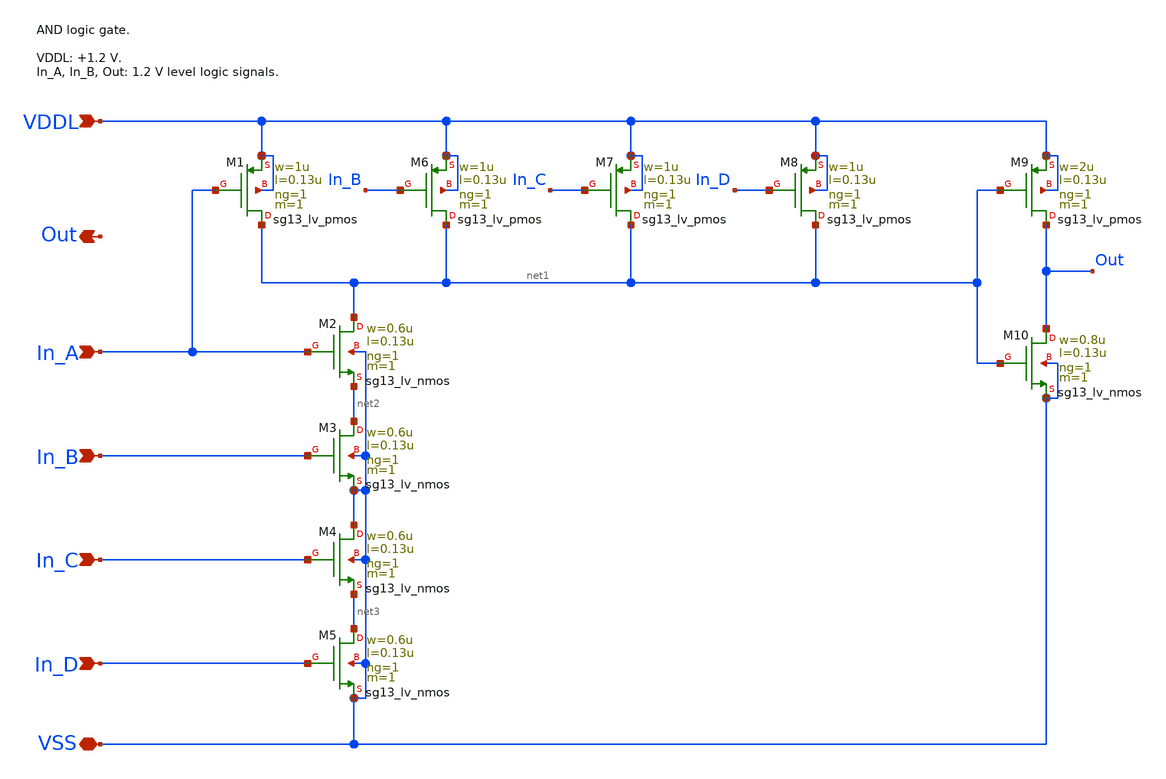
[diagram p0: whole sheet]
** sch_path: sar_adc/xschem/blocks/logic_elements/4-input_AND/4-input_AND.sch
**.subckt 4-input_AND Out VSS VDDL In_A In_B In_C In_D
*.opin Out
*.iopin VSS
*.ipin VDDL
*.ipin In_A
*.ipin In_B
*.ipin In_C
*.ipin In_D
XM1 net1 In_A VDDL VDDL sg13_lv_pmos w=1u l=0.13u ng=1 m=1 mm_ok=1
XM6 net1 In_B VDDL VDDL sg13_lv_pmos w=1u l=0.13u ng=1 m=1 mm_ok=1
XM2 net1 In_A net2 VSS sg13_lv_nmos w=0.6u l=0.13u ng=1 m=1 mm_ok=1
XM3 net2 In_B VSS VSS sg13_lv_nmos w=0.6u l=0.13u ng=1 m=1 mm_ok=1
XM9 Out net1 VDDL VDDL sg13_lv_pmos w=2u l=0.13u ng=1 m=1 mm_ok=1
XM10 Out net1 VSS VSS sg13_lv_nmos w=0.8u l=0.13u ng=1 m=1 mm_ok=1
XM4 VSS In_C net3 VSS sg13_lv_nmos w=0.6u l=0.13u ng=1 m=1 mm_ok=1
XM5 net3 In_D VSS VSS sg13_lv_nmos w=0.6u l=0.13u ng=1 m=1 mm_ok=1
XM7 net1 In_C VDDL VDDL sg13_lv_pmos w=1u l=0.13u ng=1 m=1 mm_ok=1
XM8 net1 In_D VDDL VDDL sg13_lv_pmos w=1u l=0.13u ng=1 m=1 mm_ok=1
**.ends
.end
